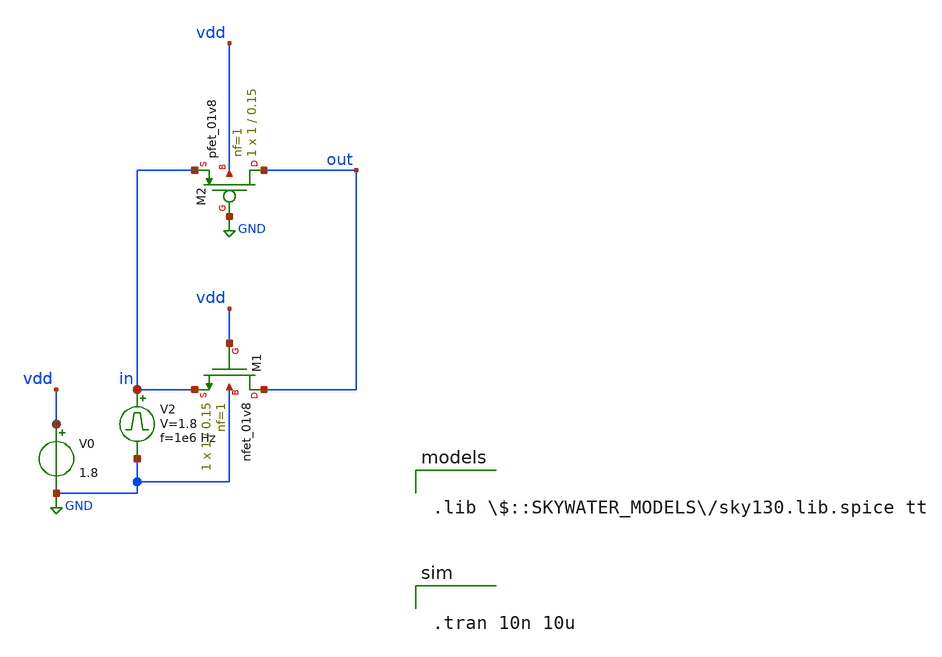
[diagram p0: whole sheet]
** sch_path: design/playground/pass-gate_1v8_tb.sch
**.subckt pass-gate_1v8_tb
XM1 out vdd in GND sky130_fd_pr__nfet_01v8 L=0.15 W=1 nf=1 ad='int((nf+1)/2) * W/nf * 0.29' as='int((nf+2)/2) * W/nf * 0.29'
+ pd='2*int((nf+1)/2) * (W/nf + 0.29)' ps='2*int((nf+2)/2) * (W/nf + 0.29)' nrd='0.29 / W' nrs='0.29 / W'
+ sa=0 sb=0 sd=0 mult=1 m=1
V0 vdd GND 1.8
V2 in GND pulse 0 1.8 '0.495/ 1e6 ' '0.01/1e6 ' '0.01/1e6 ' '0.49/1e6 ' '1/1e6 '
XM2 out GND in vdd sky130_fd_pr__pfet_01v8 L=0.15 W=1 nf=1 ad='int((nf+1)/2) * W/nf * 0.29' as='int((nf+2)/2) * W/nf * 0.29'
+ pd='2*int((nf+1)/2) * (W/nf + 0.29)' ps='2*int((nf+2)/2) * (W/nf + 0.29)' nrd='0.29 / W' nrs='0.29 / W'
+ sa=0 sb=0 sd=0 mult=1 m=1
**** begin user architecture code


.tran 10n 10u



.lib $::SKYWATER_MODELS/sky130.lib.spice tt

**** end user architecture code
**.ends
.GLOBAL GND
.end
